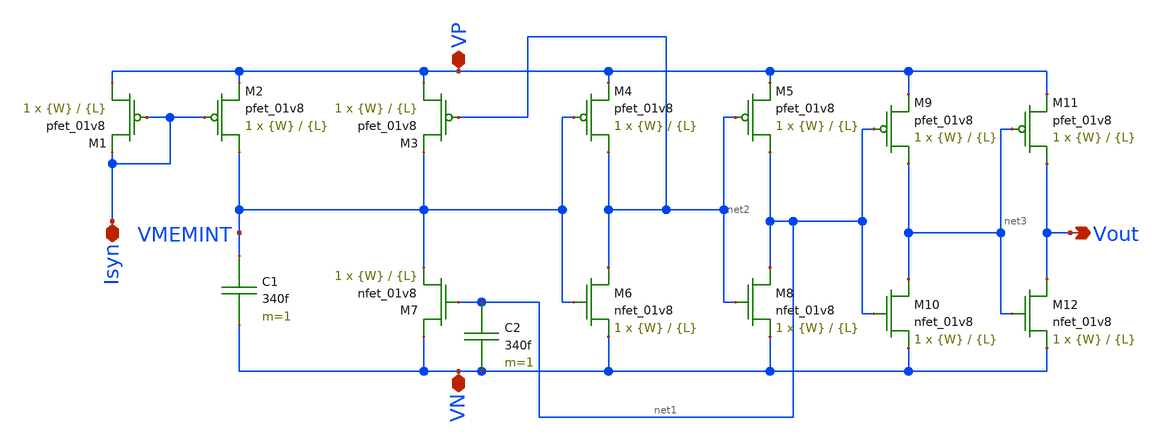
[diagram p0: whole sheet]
** sch_path: schematic/besrour_neuron.sch
**.subckt besrour_neuron VP VN Isyn Vout
*.iopin VP
*.iopin VN
*.iopin Isyn
*.opin Vout
XM1 VP Isyn Isyn VDD sky130_fd_pr__pfet_01v8 L={L} W={W} nf=1 ad='int((nf+1)/2) * W/nf * 0.29' as='int((nf+2)/2) * W/nf * 0.29'
+ pd='2*int((nf+1)/2) * (W/nf + 0.29)' ps='2*int((nf+2)/2) * (W/nf + 0.29)' nrd='0.29 / W' nrs='0.29 / W'
+ sa=0 sb=0 sd=0 mult=1 m=1
XM7 VN net1 VMEMINT GND sky130_fd_pr__nfet_01v8 L={L} W={W} nf=1 ad='int((nf+1)/2) * W/nf * 0.29' as='int((nf+2)/2) * W/nf * 0.29'
+ pd='2*int((nf+1)/2) * (W/nf + 0.29)' ps='2*int((nf+2)/2) * (W/nf + 0.29)' nrd='0.29 / W' nrs='0.29 / W'
+ sa=0 sb=0 sd=0 mult=1 m=1
XM2 VMEMINT Isyn VP VDD sky130_fd_pr__pfet_01v8 L={L} W={W} nf=1 ad='int((nf+1)/2) * W/nf * 0.29' as='int((nf+2)/2) * W/nf * 0.29'
+ pd='2*int((nf+1)/2) * (W/nf + 0.29)' ps='2*int((nf+2)/2) * (W/nf + 0.29)' nrd='0.29 / W' nrs='0.29 / W'
+ sa=0 sb=0 sd=0 mult=1 m=1
XM3 VP net2 VMEMINT VDD sky130_fd_pr__pfet_01v8 L={L} W={W} nf=1 ad='int((nf+1)/2) * W/nf * 0.29' as='int((nf+2)/2) * W/nf * 0.29'
+ pd='2*int((nf+1)/2) * (W/nf + 0.29)' ps='2*int((nf+2)/2) * (W/nf + 0.29)' nrd='0.29 / W' nrs='0.29 / W'
+ sa=0 sb=0 sd=0 mult=1 m=1
XM4 net2 VMEMINT VP VDD sky130_fd_pr__pfet_01v8 L={L} W={W} nf=1 ad='int((nf+1)/2) * W/nf * 0.29' as='int((nf+2)/2) * W/nf * 0.29'
+ pd='2*int((nf+1)/2) * (W/nf + 0.29)' ps='2*int((nf+2)/2) * (W/nf + 0.29)' nrd='0.29 / W' nrs='0.29 / W'
+ sa=0 sb=0 sd=0 mult=1 m=1
XM5 net1 net2 VP VDD sky130_fd_pr__pfet_01v8 L={L} W={W} nf=1 ad='int((nf+1)/2) * W/nf * 0.29' as='int((nf+2)/2) * W/nf * 0.29'
+ pd='2*int((nf+1)/2) * (W/nf + 0.29)' ps='2*int((nf+2)/2) * (W/nf + 0.29)' nrd='0.29 / W' nrs='0.29 / W'
+ sa=0 sb=0 sd=0 mult=1 m=1
XM6 net2 VMEMINT VN GND sky130_fd_pr__nfet_01v8 L={L} W={W} nf=1 ad='int((nf+1)/2) * W/nf * 0.29' as='int((nf+2)/2) * W/nf * 0.29'
+ pd='2*int((nf+1)/2) * (W/nf + 0.29)' ps='2*int((nf+2)/2) * (W/nf + 0.29)' nrd='0.29 / W' nrs='0.29 / W'
+ sa=0 sb=0 sd=0 mult=1 m=1
XM8 net1 net2 VN GND sky130_fd_pr__nfet_01v8 L={L} W={W} nf=1 ad='int((nf+1)/2) * W/nf * 0.29' as='int((nf+2)/2) * W/nf * 0.29'
+ pd='2*int((nf+1)/2) * (W/nf + 0.29)' ps='2*int((nf+2)/2) * (W/nf + 0.29)' nrd='0.29 / W' nrs='0.29 / W'
+ sa=0 sb=0 sd=0 mult=1 m=1
C1 VMEMINT VN 340f m=1
C2 net1 VN 340f m=1
XM9 net3 net1 VP VDD sky130_fd_pr__pfet_01v8 L={L} W={W} nf=1 ad='int((nf+1)/2) * W/nf * 0.29' as='int((nf+2)/2) * W/nf * 0.29'
+ pd='2*int((nf+1)/2) * (W/nf + 0.29)' ps='2*int((nf+2)/2) * (W/nf + 0.29)' nrd='0.29 / W' nrs='0.29 / W'
+ sa=0 sb=0 sd=0 mult=1 m=1
XM10 net3 net1 VN GND sky130_fd_pr__nfet_01v8 L={L} W={W} nf=1 ad='int((nf+1)/2) * W/nf * 0.29' as='int((nf+2)/2) * W/nf * 0.29'
+ pd='2*int((nf+1)/2) * (W/nf + 0.29)' ps='2*int((nf+2)/2) * (W/nf + 0.29)' nrd='0.29 / W' nrs='0.29 / W'
+ sa=0 sb=0 sd=0 mult=1 m=1
XM11 Vout net3 VP VDD sky130_fd_pr__pfet_01v8 L={L} W={W} nf=1 ad='int((nf+1)/2) * W/nf * 0.29' as='int((nf+2)/2) * W/nf * 0.29'
+ pd='2*int((nf+1)/2) * (W/nf + 0.29)' ps='2*int((nf+2)/2) * (W/nf + 0.29)' nrd='0.29 / W' nrs='0.29 / W'
+ sa=0 sb=0 sd=0 mult=1 m=1
XM12 Vout net3 VN GND sky130_fd_pr__nfet_01v8 L={L} W={W} nf=1 ad='int((nf+1)/2) * W/nf * 0.29' as='int((nf+2)/2) * W/nf * 0.29'
+ pd='2*int((nf+1)/2) * (W/nf + 0.29)' ps='2*int((nf+2)/2) * (W/nf + 0.29)' nrd='0.29 / W' nrs='0.29 / W'
+ sa=0 sb=0 sd=0 mult=1 m=1
**.ends
.end
